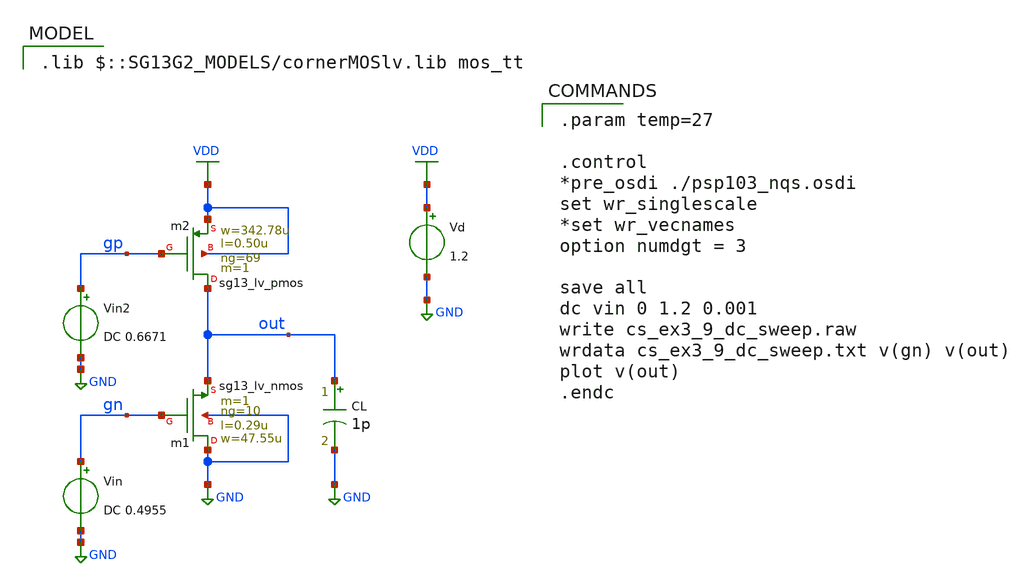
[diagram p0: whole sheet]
** sch_path: 03_design_examples/examples/src/CS_ex3_9.sch
**.subckt CS_ex3_9
Xm1 GND gn out GND sg13_lv_nmos w=47.55u l=0.29u ng=10 m=1 mm_ok=1
Vd VDD GND 1.2
CL out GND 1p m=1
Xm2 out gp VDD VDD sg13_lv_pmos w=342.78u l=0.50u ng=69 m=1 mm_ok=1
Vin gn GND DC 0.4955
Vin2 gp GND DC 0.6671
**** begin user architecture code
 .lib $::SG13G2_MODELS/cornerMOSlv.lib mos_tt


.param temp=27

.control
*pre_osdi ./psp103_nqs.osdi
set wr_singlescale
*set wr_vecnames
option numdgt = 3

save all
dc vin 0 1.2 0.001
write cs_ex3_9_dc_sweep.raw
wrdata cs_ex3_9_dc_sweep.txt v(gn) v(out)
plot v(out)
.endc


**** end user architecture code
**.ends
.GLOBAL GND
.GLOBAL VDD
.end
